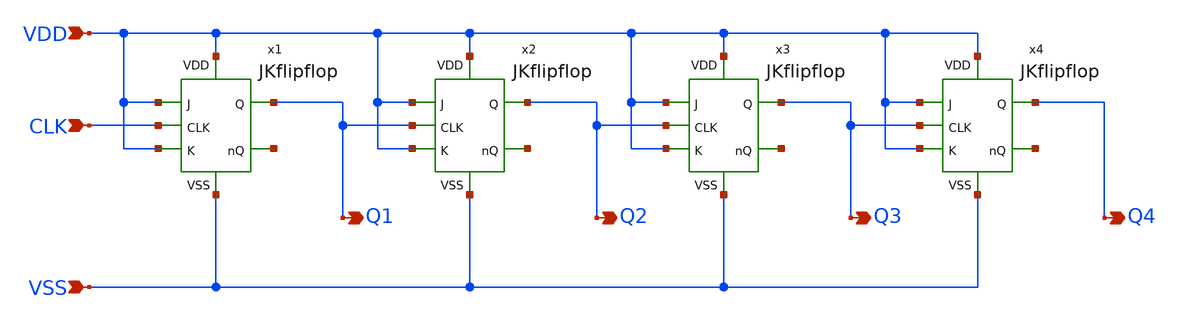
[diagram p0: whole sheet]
** sch_path: design/JNW_GR05_SKY130A/asynCounter.sch
**.subckt asynCounter VDD Q1 VSS CLK Q2 Q3 Q4
*.ipin VDD
*.opin Q1
*.ipin VSS
*.ipin CLK
*.opin Q2
*.opin Q3
*.opin Q4
x1 VDD VDD Q1 CLK net1 VDD VSS JKflipflop
x2 VDD VDD Q2 Q1 net2 VDD VSS JKflipflop
x3 VDD VDD Q3 Q2 net3 VDD VSS JKflipflop
x4 VDD VDD Q4 Q3 net4 VDD VSS JKflipflop
**.ends
.end
